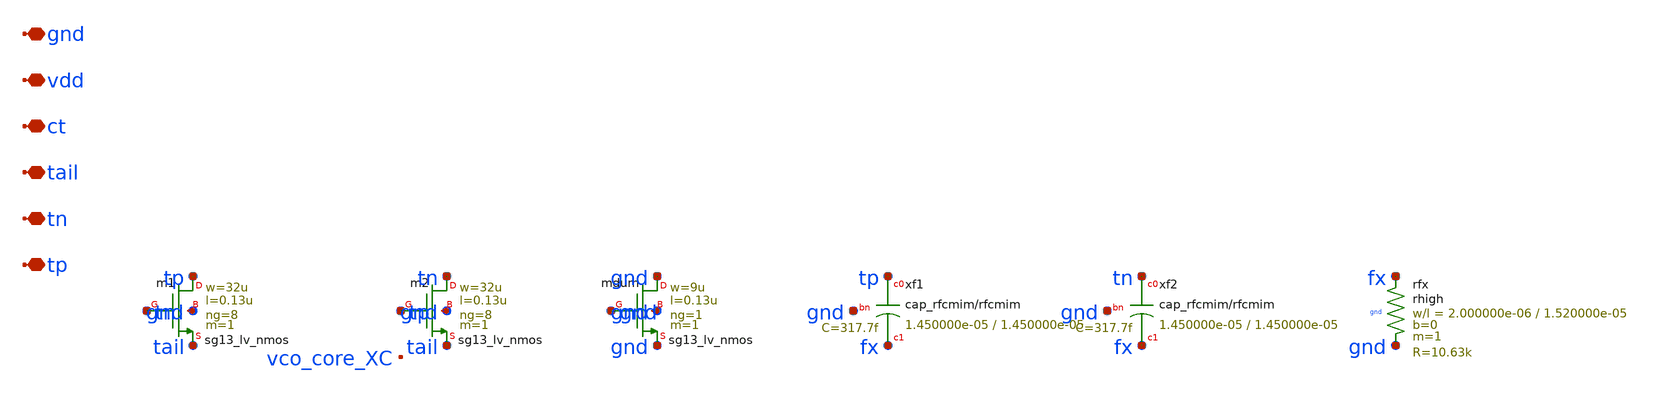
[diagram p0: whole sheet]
** sch_path: analog/vco/sch/vco_core.sch
**.subckt vco_core tp tn tail ct vdd gnd
*.iopin tp
*.iopin tn
*.iopin tail
*.iopin ct
*.iopin vdd
*.iopin gnd
Xm1 tp tn tail gnd sg13_lv_nmos w=32u l=0.13u ng=8 m=1 mm_ok=1
Xm2 tn tp tail gnd sg13_lv_nmos w=32u l=0.13u ng=8 m=1 mm_ok=1
Xmdum gnd gnd gnd gnd sg13_lv_nmos w=9u l=0.13u ng=1 m=1 mm_ok=1
Xxf1 tp fx gnd cap_rfcmim w=1.450000e-05 l=1.450000e-05 wfeed=5.0e-6 m=1 mm_ok=1
Xxf2 tn fx gnd cap_rfcmim w=1.450000e-05 l=1.450000e-05 wfeed=5.0e-6 m=1 mm_ok=1
Xrfx fx gnd gnd rhigh w=2.000000e-06 l=1.520000e-05 m=1 b=0 mm_ok=1
**.ends
.end
